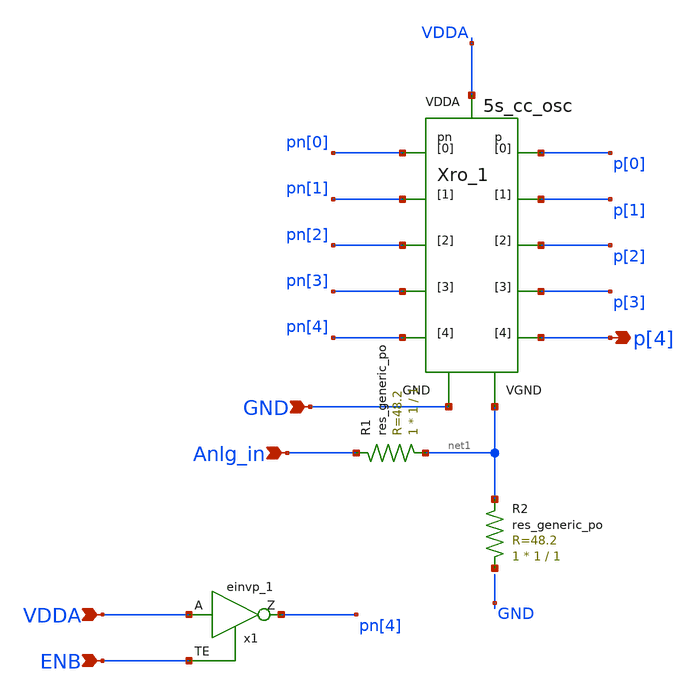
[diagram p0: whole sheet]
** sch_path: xschem/lib/ALib_VCO.sch
**.subckt ALib_VCO Anlg_in VDDA ENB p[4] GND
*.ipin Anlg_in
*.ipin VDDA
*.ipin ENB
*.opin p[4]
*.ipin GND
Xro_1 net1 VDDA p[0] p[1] p[2] p[3] p[4] pn[0] pn[1] pn[2] pn[3] pn[4] GND 5s_cc_osc
x1 VDDA ENB VGND VNB VPB VPWR pn[4] sky130_fd_sc_hd__einvp_1
XR1 net1 Anlg_in sky130_fd_pr__res_generic_po W=1 L=1 m=1
XR2 net2 net1 sky130_fd_pr__res_generic_po W=1 L=1 m=1
**.ends
.end
